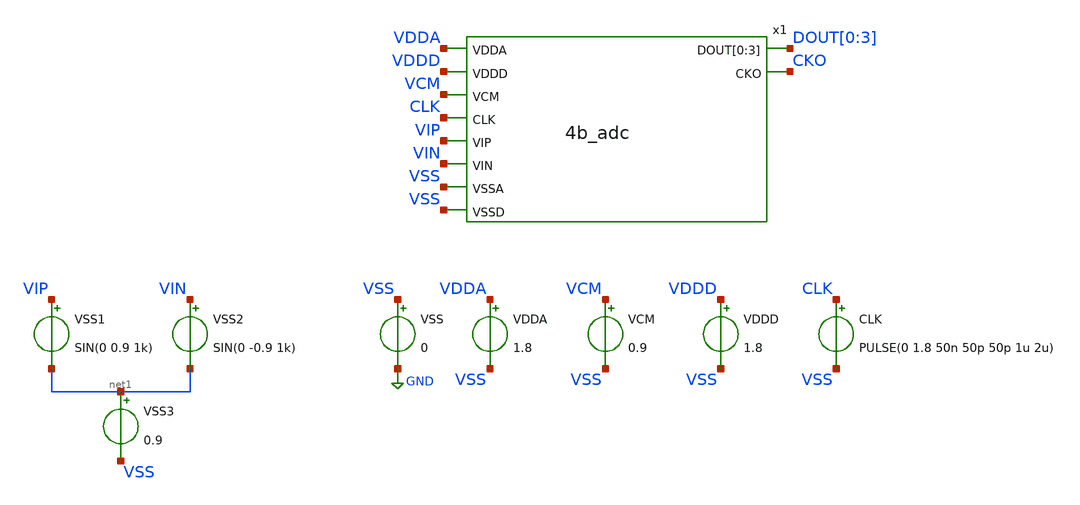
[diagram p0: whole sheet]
** sch_path: xschem/adc_tb.sch
**.subckt adc_tb
x1 VDDA VDDD VCM CLK VIP VIN VSS VSS DOUT[0] DOUT[1] DOUT[2] DOUT[3] CKO 4b_adc
VSS VSS GND 0
VDDA VDDA VSS 1.8
VDDD VDDD VSS 1.8
CLK CLK VSS PULSE(0 1.8 50n 50p 50p 1u 2u)
VCM VCM VSS 0.9
VSS1 VIP net1 SIN(0 0.9 1k)
VSS2 VIN net1 SIN(0 -0.9 1k)
VSS3 net1 VSS 0.9
**** begin user architecture code

** opencircuitdesign pdks install
.lib $::SKYWATER_MODELS/sky130.lib.spice tt
.include /usr/local/share/pdk/sky130A/libs.ref/sky130_fd_sc_hd/spice/sky130_fd_sc_hd.spice



.option wnflag=0
.option savecurrents
.control
tran 1n 1m
plot DOUT[0:3]
.endc

**** end user architecture code
**.ends
.GLOBAL GND
.end
